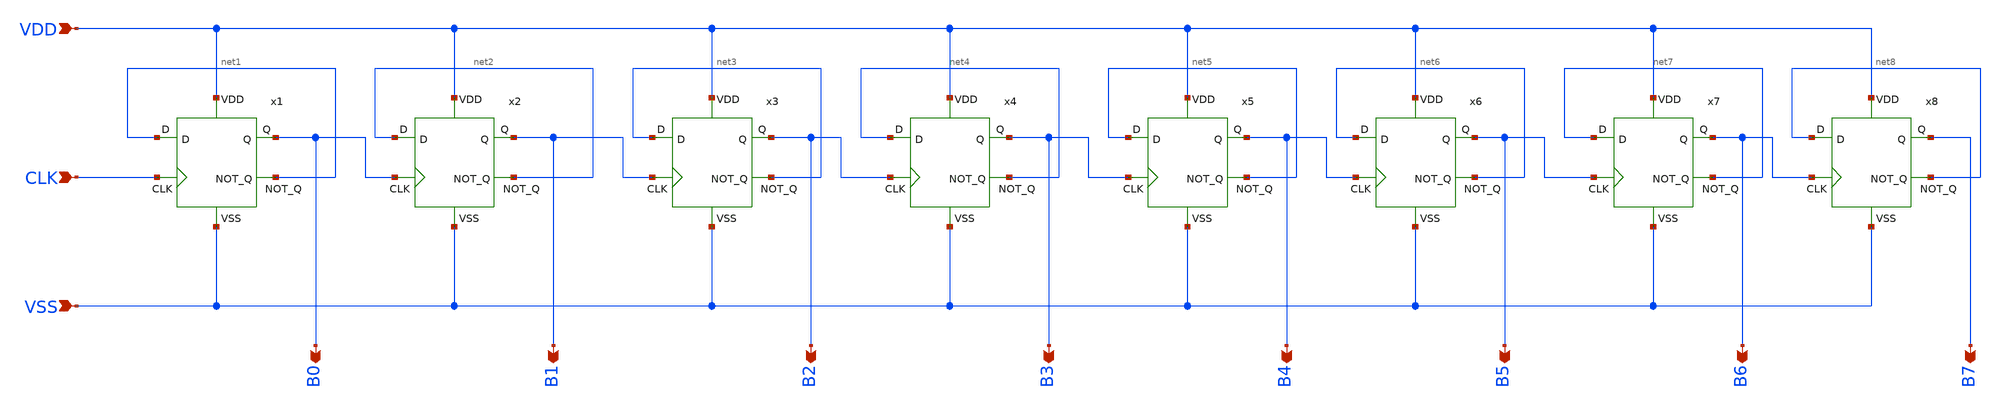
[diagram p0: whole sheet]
** sch_path: design/JNW_GR03_SKY130A/JNW_GR03_8BCOUNTER.sch
**.subckt JNW_GR03_8BCOUNTER VDD VSS CLK B0 B1 B2 B3 B4 B5 B6 B7
*.ipin VDD
*.ipin VSS
*.ipin CLK
*.opin B0
*.opin B1
*.opin B2
*.opin B3
*.opin B4
*.opin B5
*.opin B6
*.opin B7
x1 VDD B0 net1 net1 CLK VSS JNW_GR03_DFLIPFLOP_R
x2 VDD B1 net2 net2 B0 VSS JNW_GR03_DFLIPFLOP_R
x3 VDD B2 net3 net3 B1 VSS JNW_GR03_DFLIPFLOP_R
x4 VDD B3 net4 net4 B2 VSS JNW_GR03_DFLIPFLOP_R
x5 VDD B4 net5 net5 B3 VSS JNW_GR03_DFLIPFLOP_R
x6 VDD B5 net6 net6 B4 VSS JNW_GR03_DFLIPFLOP_R
x7 VDD B6 net7 net7 B5 VSS JNW_GR03_DFLIPFLOP_R
x8 VDD B7 net8 net8 B6 VSS JNW_GR03_DFLIPFLOP_R
**.ends
.end
